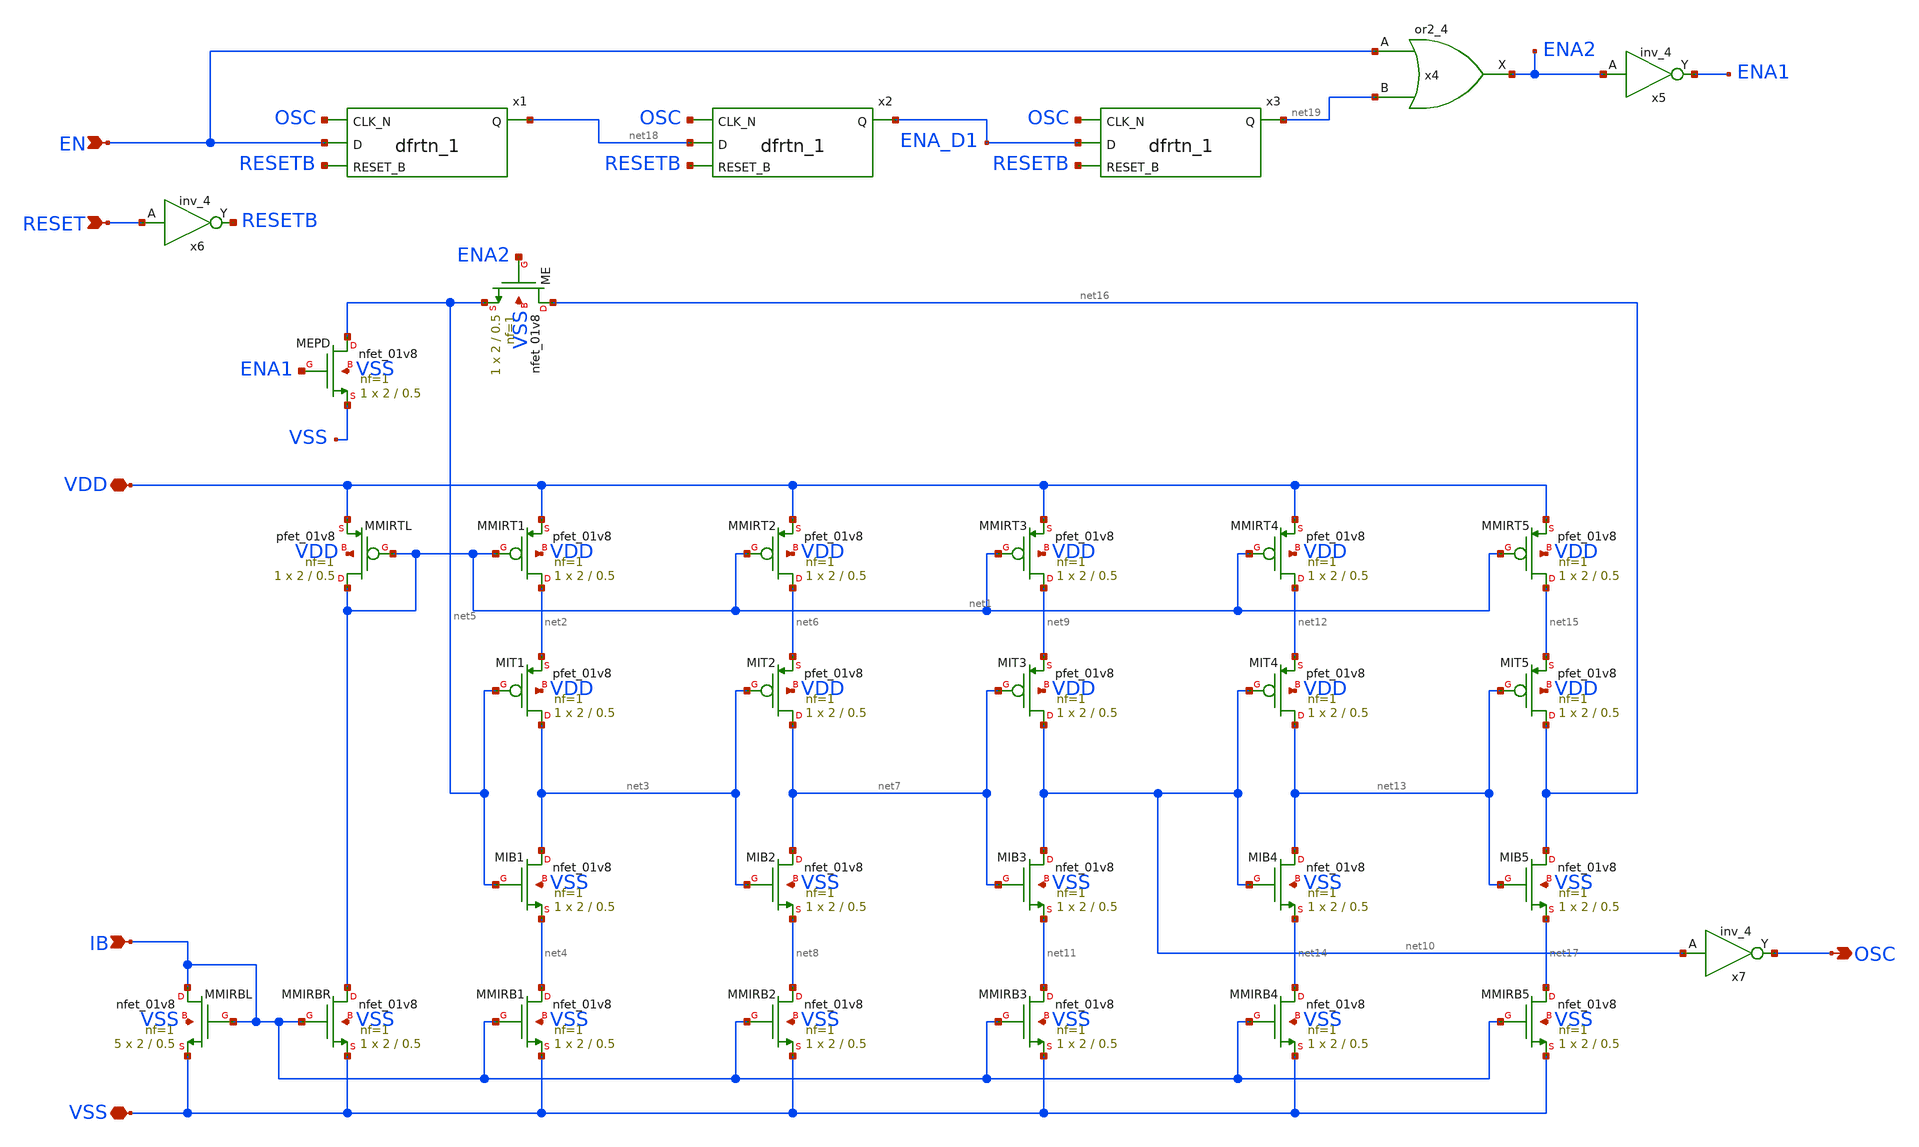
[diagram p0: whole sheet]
** sch_path: tt08/ip/riosc/xschem/riosc.sch
**.subckt riosc VSS VDD IB OSC EN RESET
*.iopin VSS
*.iopin VDD
*.ipin IB
*.opin OSC
*.ipin EN
*.ipin RESET
XMMIRTL net1 net1 VDD VDD sky130_fd_pr__pfet_01v8 L=0.5 W=2 nf=1 ad='int((nf+1)/2) * W/nf * 0.29' as='int((nf+2)/2) * W/nf * 0.29'
+ pd='2*int((nf+1)/2) * (W/nf + 0.29)' ps='2*int((nf+2)/2) * (W/nf + 0.29)' nrd='0.29 / W' nrs='0.29 / W'
+ sa=0 sb=0 sd=0 mult=1 m=1
XMMIRBL IB IB VSS VSS sky130_fd_pr__nfet_01v8 L=0.5 W=2 nf=1 ad='int((nf+1)/2) * W/nf * 0.29' as='int((nf+2)/2) * W/nf * 0.29'
+ pd='2*int((nf+1)/2) * (W/nf + 0.29)' ps='2*int((nf+2)/2) * (W/nf + 0.29)' nrd='0.29 / W' nrs='0.29 / W'
+ sa=0 sb=0 sd=0 mult=5 m=5
XMMIRBR net1 IB VSS VSS sky130_fd_pr__nfet_01v8 L=0.5 W=2 nf=1 ad='int((nf+1)/2) * W/nf * 0.29' as='int((nf+2)/2) * W/nf * 0.29'
+ pd='2*int((nf+1)/2) * (W/nf + 0.29)' ps='2*int((nf+2)/2) * (W/nf + 0.29)' nrd='0.29 / W' nrs='0.29 / W'
+ sa=0 sb=0 sd=0 mult=1 m=1
XMMIRT1 net2 net1 VDD VDD sky130_fd_pr__pfet_01v8 L=0.5 W=2 nf=1 ad='int((nf+1)/2) * W/nf * 0.29' as='int((nf+2)/2) * W/nf * 0.29'
+ pd='2*int((nf+1)/2) * (W/nf + 0.29)' ps='2*int((nf+2)/2) * (W/nf + 0.29)' nrd='0.29 / W' nrs='0.29 / W'
+ sa=0 sb=0 sd=0 mult=1 m=1
XMMIRB1 net4 IB VSS VSS sky130_fd_pr__nfet_01v8 L=0.5 W=2 nf=1 ad='int((nf+1)/2) * W/nf * 0.29' as='int((nf+2)/2) * W/nf * 0.29'
+ pd='2*int((nf+1)/2) * (W/nf + 0.29)' ps='2*int((nf+2)/2) * (W/nf + 0.29)' nrd='0.29 / W' nrs='0.29 / W'
+ sa=0 sb=0 sd=0 mult=1 m=1
XMIT1 net3 net5 net2 VDD sky130_fd_pr__pfet_01v8 L=0.5 W=2 nf=1 ad='int((nf+1)/2) * W/nf * 0.29' as='int((nf+2)/2) * W/nf * 0.29'
+ pd='2*int((nf+1)/2) * (W/nf + 0.29)' ps='2*int((nf+2)/2) * (W/nf + 0.29)' nrd='0.29 / W' nrs='0.29 / W'
+ sa=0 sb=0 sd=0 mult=1 m=1
XMIB1 net3 net5 net4 VSS sky130_fd_pr__nfet_01v8 L=0.5 W=2 nf=1 ad='int((nf+1)/2) * W/nf * 0.29' as='int((nf+2)/2) * W/nf * 0.29'
+ pd='2*int((nf+1)/2) * (W/nf + 0.29)' ps='2*int((nf+2)/2) * (W/nf + 0.29)' nrd='0.29 / W' nrs='0.29 / W'
+ sa=0 sb=0 sd=0 mult=1 m=1
XMMIRT2 net6 net1 VDD VDD sky130_fd_pr__pfet_01v8 L=0.5 W=2 nf=1 ad='int((nf+1)/2) * W/nf * 0.29' as='int((nf+2)/2) * W/nf * 0.29'
+ pd='2*int((nf+1)/2) * (W/nf + 0.29)' ps='2*int((nf+2)/2) * (W/nf + 0.29)' nrd='0.29 / W' nrs='0.29 / W'
+ sa=0 sb=0 sd=0 mult=1 m=1
XMMIRB2 net8 IB VSS VSS sky130_fd_pr__nfet_01v8 L=0.5 W=2 nf=1 ad='int((nf+1)/2) * W/nf * 0.29' as='int((nf+2)/2) * W/nf * 0.29'
+ pd='2*int((nf+1)/2) * (W/nf + 0.29)' ps='2*int((nf+2)/2) * (W/nf + 0.29)' nrd='0.29 / W' nrs='0.29 / W'
+ sa=0 sb=0 sd=0 mult=1 m=1
XMIT2 net7 net3 net6 VDD sky130_fd_pr__pfet_01v8 L=0.5 W=2 nf=1 ad='int((nf+1)/2) * W/nf * 0.29' as='int((nf+2)/2) * W/nf * 0.29'
+ pd='2*int((nf+1)/2) * (W/nf + 0.29)' ps='2*int((nf+2)/2) * (W/nf + 0.29)' nrd='0.29 / W' nrs='0.29 / W'
+ sa=0 sb=0 sd=0 mult=1 m=1
XMIB2 net7 net3 net8 VSS sky130_fd_pr__nfet_01v8 L=0.5 W=2 nf=1 ad='int((nf+1)/2) * W/nf * 0.29' as='int((nf+2)/2) * W/nf * 0.29'
+ pd='2*int((nf+1)/2) * (W/nf + 0.29)' ps='2*int((nf+2)/2) * (W/nf + 0.29)' nrd='0.29 / W' nrs='0.29 / W'
+ sa=0 sb=0 sd=0 mult=1 m=1
XMMIRT3 net9 net1 VDD VDD sky130_fd_pr__pfet_01v8 L=0.5 W=2 nf=1 ad='int((nf+1)/2) * W/nf * 0.29' as='int((nf+2)/2) * W/nf * 0.29'
+ pd='2*int((nf+1)/2) * (W/nf + 0.29)' ps='2*int((nf+2)/2) * (W/nf + 0.29)' nrd='0.29 / W' nrs='0.29 / W'
+ sa=0 sb=0 sd=0 mult=1 m=1
XMMIRB3 net11 IB VSS VSS sky130_fd_pr__nfet_01v8 L=0.5 W=2 nf=1 ad='int((nf+1)/2) * W/nf * 0.29' as='int((nf+2)/2) * W/nf * 0.29'
+ pd='2*int((nf+1)/2) * (W/nf + 0.29)' ps='2*int((nf+2)/2) * (W/nf + 0.29)' nrd='0.29 / W' nrs='0.29 / W'
+ sa=0 sb=0 sd=0 mult=1 m=1
XMIT3 net10 net7 net9 VDD sky130_fd_pr__pfet_01v8 L=0.5 W=2 nf=1 ad='int((nf+1)/2) * W/nf * 0.29' as='int((nf+2)/2) * W/nf * 0.29'
+ pd='2*int((nf+1)/2) * (W/nf + 0.29)' ps='2*int((nf+2)/2) * (W/nf + 0.29)' nrd='0.29 / W' nrs='0.29 / W'
+ sa=0 sb=0 sd=0 mult=1 m=1
XMIB3 net10 net7 net11 VSS sky130_fd_pr__nfet_01v8 L=0.5 W=2 nf=1 ad='int((nf+1)/2) * W/nf * 0.29' as='int((nf+2)/2) * W/nf * 0.29'
+ pd='2*int((nf+1)/2) * (W/nf + 0.29)' ps='2*int((nf+2)/2) * (W/nf + 0.29)' nrd='0.29 / W' nrs='0.29 / W'
+ sa=0 sb=0 sd=0 mult=1 m=1
XMMIRT4 net12 net1 VDD VDD sky130_fd_pr__pfet_01v8 L=0.5 W=2 nf=1 ad='int((nf+1)/2) * W/nf * 0.29' as='int((nf+2)/2) * W/nf * 0.29'
+ pd='2*int((nf+1)/2) * (W/nf + 0.29)' ps='2*int((nf+2)/2) * (W/nf + 0.29)' nrd='0.29 / W' nrs='0.29 / W'
+ sa=0 sb=0 sd=0 mult=1 m=1
XMMIRB4 net14 IB VSS VSS sky130_fd_pr__nfet_01v8 L=0.5 W=2 nf=1 ad='int((nf+1)/2) * W/nf * 0.29' as='int((nf+2)/2) * W/nf * 0.29'
+ pd='2*int((nf+1)/2) * (W/nf + 0.29)' ps='2*int((nf+2)/2) * (W/nf + 0.29)' nrd='0.29 / W' nrs='0.29 / W'
+ sa=0 sb=0 sd=0 mult=1 m=1
XMIT4 net13 net10 net12 VDD sky130_fd_pr__pfet_01v8 L=0.5 W=2 nf=1 ad='int((nf+1)/2) * W/nf * 0.29' as='int((nf+2)/2) * W/nf * 0.29'
+ pd='2*int((nf+1)/2) * (W/nf + 0.29)' ps='2*int((nf+2)/2) * (W/nf + 0.29)' nrd='0.29 / W' nrs='0.29 / W'
+ sa=0 sb=0 sd=0 mult=1 m=1
XMIB4 net13 net10 net14 VSS sky130_fd_pr__nfet_01v8 L=0.5 W=2 nf=1 ad='int((nf+1)/2) * W/nf * 0.29' as='int((nf+2)/2) * W/nf * 0.29'
+ pd='2*int((nf+1)/2) * (W/nf + 0.29)' ps='2*int((nf+2)/2) * (W/nf + 0.29)' nrd='0.29 / W' nrs='0.29 / W'
+ sa=0 sb=0 sd=0 mult=1 m=1
XMMIRT5 net15 net1 VDD VDD sky130_fd_pr__pfet_01v8 L=0.5 W=2 nf=1 ad='int((nf+1)/2) * W/nf * 0.29' as='int((nf+2)/2) * W/nf * 0.29'
+ pd='2*int((nf+1)/2) * (W/nf + 0.29)' ps='2*int((nf+2)/2) * (W/nf + 0.29)' nrd='0.29 / W' nrs='0.29 / W'
+ sa=0 sb=0 sd=0 mult=1 m=1
XMMIRB5 net17 IB VSS VSS sky130_fd_pr__nfet_01v8 L=0.5 W=2 nf=1 ad='int((nf+1)/2) * W/nf * 0.29' as='int((nf+2)/2) * W/nf * 0.29'
+ pd='2*int((nf+1)/2) * (W/nf + 0.29)' ps='2*int((nf+2)/2) * (W/nf + 0.29)' nrd='0.29 / W' nrs='0.29 / W'
+ sa=0 sb=0 sd=0 mult=1 m=1
XMIT5 net16 net13 net15 VDD sky130_fd_pr__pfet_01v8 L=0.5 W=2 nf=1 ad='int((nf+1)/2) * W/nf * 0.29' as='int((nf+2)/2) * W/nf * 0.29'
+ pd='2*int((nf+1)/2) * (W/nf + 0.29)' ps='2*int((nf+2)/2) * (W/nf + 0.29)' nrd='0.29 / W' nrs='0.29 / W'
+ sa=0 sb=0 sd=0 mult=1 m=1
XMIB5 net16 net13 net17 VSS sky130_fd_pr__nfet_01v8 L=0.5 W=2 nf=1 ad='int((nf+1)/2) * W/nf * 0.29' as='int((nf+2)/2) * W/nf * 0.29'
+ pd='2*int((nf+1)/2) * (W/nf + 0.29)' ps='2*int((nf+2)/2) * (W/nf + 0.29)' nrd='0.29 / W' nrs='0.29 / W'
+ sa=0 sb=0 sd=0 mult=1 m=1
XME net16 ENA2 net5 VSS sky130_fd_pr__nfet_01v8 L=0.5 W=2 nf=1 ad='int((nf+1)/2) * W/nf * 0.29' as='int((nf+2)/2) * W/nf * 0.29'
+ pd='2*int((nf+1)/2) * (W/nf + 0.29)' ps='2*int((nf+2)/2) * (W/nf + 0.29)' nrd='0.29 / W' nrs='0.29 / W'
+ sa=0 sb=0 sd=0 mult=1 m=1
XMEPD net5 ENA1 VSS VSS sky130_fd_pr__nfet_01v8 L=0.5 W=2 nf=1 ad='int((nf+1)/2) * W/nf * 0.29' as='int((nf+2)/2) * W/nf * 0.29'
+ pd='2*int((nf+1)/2) * (W/nf + 0.29)' ps='2*int((nf+2)/2) * (W/nf + 0.29)' nrd='0.29 / W' nrs='0.29 / W'
+ sa=0 sb=0 sd=0 mult=1 m=1
x6 RESET VSS VSS VDD VDD RESETB sky130_fd_sc_hd__inv_4
x5 ENA2 VSS VSS VDD VDD ENA1 sky130_fd_sc_hd__inv_4
x4 EN net19 VSS VSS VDD VDD ENA2 sky130_fd_sc_hd__or2_4
x1 OSC EN RESETB VSS VSS VDD VDD net18 sky130_fd_sc_hd__dfrtn_1
x2 OSC net18 RESETB VSS VSS VDD VDD ENA_D1 sky130_fd_sc_hd__dfrtn_1
x3 OSC ENA_D1 RESETB VSS VSS VDD VDD net19 sky130_fd_sc_hd__dfrtn_1
x7 net10 VSS VSS VDD VDD OSC sky130_fd_sc_hd__inv_4
**** begin user architecture code

.include $::SKYWATER_STDCELLS/sky130_fd_sc_hd.spice

**** end user architecture code
**.ends
.end
